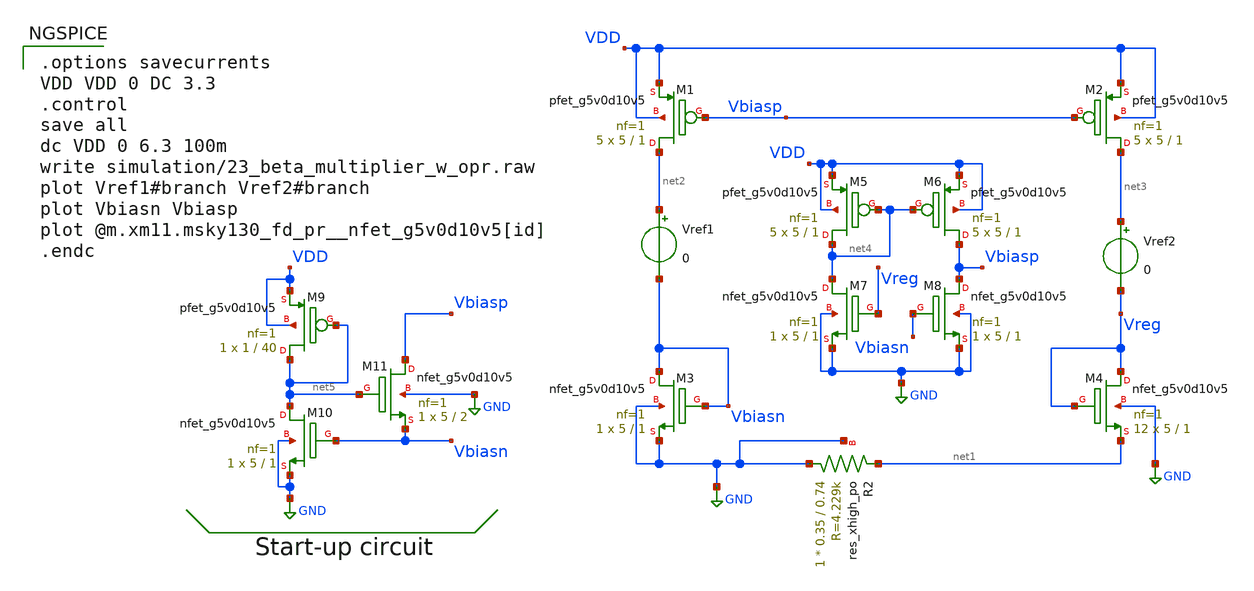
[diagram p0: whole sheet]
** sch_path: xschem/23_beta_multiplier_w_opr.sch
**.subckt 23_beta_multiplier_w_opr
XM1 net2 Vbiasp VDD VDD sky130_fd_pr__pfet_g5v0d10v5 L=1 W=5 nf=1 ad='int((nf+1)/2) * W/nf * 0.29' as='int((nf+2)/2) * W/nf * 0.29'
+ pd='2*int((nf+1)/2) * (W/nf + 0.29)' ps='2*int((nf+2)/2) * (W/nf + 0.29)' nrd='0.29 / W' nrs='0.29 / W'
+ sa=0 sb=0 sd=0 mult=5 m=5
XM3 Vbiasn Vbiasn GND GND sky130_fd_pr__nfet_g5v0d10v5 L=1 W=5 nf=1 ad='int((nf+1)/2) * W/nf * 0.29'
+ as='int((nf+2)/2) * W/nf * 0.29' pd='2*int((nf+1)/2) * (W/nf + 0.29)' ps='2*int((nf+2)/2) * (W/nf + 0.29)'
+ nrd='0.29 / W' nrs='0.29 / W' sa=0 sb=0 sd=0 mult=1 m=1
XM2 net3 Vbiasp VDD VDD sky130_fd_pr__pfet_g5v0d10v5 L=1 W=5 nf=1 ad='int((nf+1)/2) * W/nf * 0.29' as='int((nf+2)/2) * W/nf * 0.29'
+ pd='2*int((nf+1)/2) * (W/nf + 0.29)' ps='2*int((nf+2)/2) * (W/nf + 0.29)' nrd='0.29 / W' nrs='0.29 / W'
+ sa=0 sb=0 sd=0 mult=5 m=5
XM4 Vreg Vreg net1 GND sky130_fd_pr__nfet_g5v0d10v5 L=1 W=5 nf=1 ad='int((nf+1)/2) * W/nf * 0.29' as='int((nf+2)/2) * W/nf * 0.29'
+ pd='2*int((nf+1)/2) * (W/nf + 0.29)' ps='2*int((nf+2)/2) * (W/nf + 0.29)' nrd='0.29 / W' nrs='0.29 / W'
+ sa=0 sb=0 sd=0 mult=12 m=12
Vref1 net2 Vbiasn 0
Vref2 net3 Vreg 0
XR2 GND net1 GND sky130_fd_pr__res_xhigh_po W=0.35 L=0.74 mult=1 m=1
XM5 net4 net4 VDD VDD sky130_fd_pr__pfet_g5v0d10v5 L=1 W=5 nf=1 ad='int((nf+1)/2) * W/nf * 0.29' as='int((nf+2)/2) * W/nf * 0.29'
+ pd='2*int((nf+1)/2) * (W/nf + 0.29)' ps='2*int((nf+2)/2) * (W/nf + 0.29)' nrd='0.29 / W' nrs='0.29 / W'
+ sa=0 sb=0 sd=0 mult=5 m=5
XM6 Vbiasp net4 VDD VDD sky130_fd_pr__pfet_g5v0d10v5 L=1 W=5 nf=1 ad='int((nf+1)/2) * W/nf * 0.29' as='int((nf+2)/2) * W/nf * 0.29'
+ pd='2*int((nf+1)/2) * (W/nf + 0.29)' ps='2*int((nf+2)/2) * (W/nf + 0.29)' nrd='0.29 / W' nrs='0.29 / W'
+ sa=0 sb=0 sd=0 mult=5 m=5
XM7 net4 Vreg GND GND sky130_fd_pr__nfet_g5v0d10v5 L=1 W=5 nf=1 ad='int((nf+1)/2) * W/nf * 0.29' as='int((nf+2)/2) * W/nf * 0.29'
+ pd='2*int((nf+1)/2) * (W/nf + 0.29)' ps='2*int((nf+2)/2) * (W/nf + 0.29)' nrd='0.29 / W' nrs='0.29 / W'
+ sa=0 sb=0 sd=0 mult=1 m=1
XM8 Vbiasp Vbiasn GND GND sky130_fd_pr__nfet_g5v0d10v5 L=1 W=5 nf=1 ad='int((nf+1)/2) * W/nf * 0.29'
+ as='int((nf+2)/2) * W/nf * 0.29' pd='2*int((nf+1)/2) * (W/nf + 0.29)' ps='2*int((nf+2)/2) * (W/nf + 0.29)'
+ nrd='0.29 / W' nrs='0.29 / W' sa=0 sb=0 sd=0 mult=1 m=1
XM9 net5 net5 VDD VDD sky130_fd_pr__pfet_g5v0d10v5 L=40 W=1 nf=1 ad='int((nf+1)/2) * W/nf * 0.29' as='int((nf+2)/2) * W/nf * 0.29'
+ pd='2*int((nf+1)/2) * (W/nf + 0.29)' ps='2*int((nf+2)/2) * (W/nf + 0.29)' nrd='0.29 / W' nrs='0.29 / W'
+ sa=0 sb=0 sd=0 mult=1 m=1
XM10 net5 Vbiasn GND GND sky130_fd_pr__nfet_g5v0d10v5 L=1 W=5 nf=1 ad='int((nf+1)/2) * W/nf * 0.29' as='int((nf+2)/2) * W/nf * 0.29'
+ pd='2*int((nf+1)/2) * (W/nf + 0.29)' ps='2*int((nf+2)/2) * (W/nf + 0.29)' nrd='0.29 / W' nrs='0.29 / W'
+ sa=0 sb=0 sd=0 mult=1 m=1
XM11 Vbiasp net5 Vbiasn GND sky130_fd_pr__nfet_g5v0d10v5 L=2 W=5 nf=1 ad='int((nf+1)/2) * W/nf * 0.29'
+ as='int((nf+2)/2) * W/nf * 0.29' pd='2*int((nf+1)/2) * (W/nf + 0.29)' ps='2*int((nf+2)/2) * (W/nf + 0.29)'
+ nrd='0.29 / W' nrs='0.29 / W' sa=0 sb=0 sd=0 mult=1 m=1
**** begin user architecture code

.options savecurrents
VDD VDD 0 DC 3.3
.control
save all
dc VDD 0 6.3 100m
write simulation/23_beta_multiplier_w_opr.raw
plot Vref1#branch Vref2#branch
plot Vbiasn Vbiasp
plot @m.xm11.msky130_fd_pr__nfet_g5v0d10v5[id]
.endc



** opencircuitdesign pdks install
.lib $::SKYWATER_MODELS/sky130.lib.spice tt


**** end user architecture code
**.ends
.GLOBAL GND
.end
